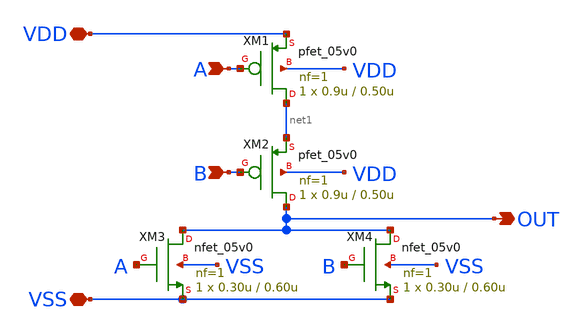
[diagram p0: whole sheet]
** sch_path: designs/relaxation-oscillator/nor.sch
**.subckt nor A B VDD VSS OUT
*.ipin A
*.ipin B
*.iopin VDD
*.iopin VSS
*.opin OUT
XM1 net1 A VDD VDD pfet_05v0 L=0.50u W=0.9u nf=1 ad='int((nf+1)/2) * W/nf * 0.18u' as='int((nf+2)/2) * W/nf * 0.18u'
+ pd='2*int((nf+1)/2) * (W/nf + 0.18u)' ps='2*int((nf+2)/2) * (W/nf + 0.18u)' nrd='0.18u / W' nrs='0.18u / W'
+ sa=0 sb=0 sd=0 m=1
XM2 OUT B net1 VDD pfet_05v0 L=0.50u W=0.9u nf=1 ad='int((nf+1)/2) * W/nf * 0.18u' as='int((nf+2)/2) * W/nf * 0.18u'
+ pd='2*int((nf+1)/2) * (W/nf + 0.18u)' ps='2*int((nf+2)/2) * (W/nf + 0.18u)' nrd='0.18u / W' nrs='0.18u / W'
+ sa=0 sb=0 sd=0 m=1
XM3 OUT A VSS VSS nfet_05v0 L=0.60u W=0.30u nf=1 ad='int((nf+1)/2) * W/nf * 0.18u' as='int((nf+2)/2) * W/nf * 0.18u'
+ pd='2*int((nf+1)/2) * (W/nf + 0.18u)' ps='2*int((nf+2)/2) * (W/nf + 0.18u)' nrd='0.18u / W' nrs='0.18u / W'
+ sa=0 sb=0 sd=0 m=1
XM4 OUT B VSS VSS nfet_05v0 L=0.60u W=0.30u nf=1 ad='int((nf+1)/2) * W/nf * 0.18u' as='int((nf+2)/2) * W/nf * 0.18u'
+ pd='2*int((nf+1)/2) * (W/nf + 0.18u)' ps='2*int((nf+2)/2) * (W/nf + 0.18u)' nrd='0.18u / W' nrs='0.18u / W'
+ sa=0 sb=0 sd=0 m=1
**.ends
.end
